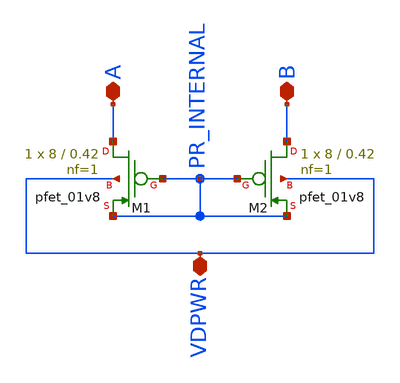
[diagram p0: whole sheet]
** sch_path: xschem/pseudo_res.sch
**.subckt pseudo_res A B VDPWR
*.iopin A
*.iopin B
*.iopin VDPWR
XM1 A PR_INTERNAL PR_INTERNAL VDPWR sky130_fd_pr__pfet_01v8 L=0.42 W=8 nf=1 ad='int((1 + 1)/2) * 8 / 1 * 0.29'
+ as='int((1 + 2)/2) * 8 / 1 * 0.29' pd='2*int((1 + 1)/2) * (8 / 1 + 0.29)' ps='2*int((1 + 2)/2) * (8 / 1 + 0.29)'
+ nrd='0.29 / 8 ' nrs='0.29 / 8 ' sa=0 sb=0 sd=0 mult=1 m=1
XM2 B PR_INTERNAL PR_INTERNAL VDPWR sky130_fd_pr__pfet_01v8 L=0.42 W=8 nf=1 ad='int((1 + 1)/2) * 8 / 1 * 0.29'
+ as='int((1 + 2)/2) * 8 / 1 * 0.29' pd='2*int((1 + 1)/2) * (8 / 1 + 0.29)' ps='2*int((1 + 2)/2) * (8 / 1 + 0.29)'
+ nrd='0.29 / 8 ' nrs='0.29 / 8 ' sa=0 sb=0 sd=0 mult=1 m=1
**.ends
.end
